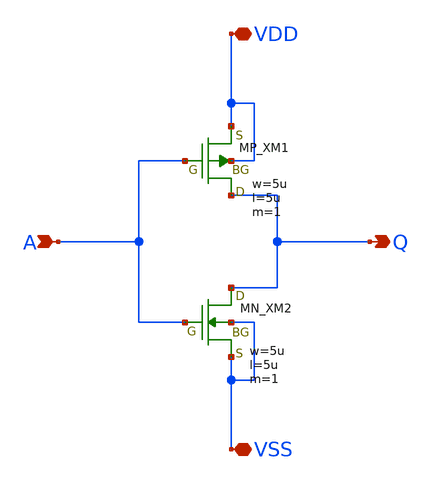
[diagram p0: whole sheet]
** sch_path: schematic/20250924_OSS_Workshop/Qdai/inverter_MUX_02/inv_NaokiFukushima.sch
**.subckt inv_NaokiFukushima VDD VSS A Q
*.iopin VDD
*.iopin VSS
*.ipin A
*.opin Q
XM1 Q A VDD VDD PMOS w=5u l=5u as=0 ad=0 ps=0 pd=0 nrd=0 nrs=0 m=1
XM2 Q A VSS VSS NMOS w=5u l=5u as=0 ad=0 ps=0 pd=0 nrd=0 nrs=0 m=1
**.ends
.end
